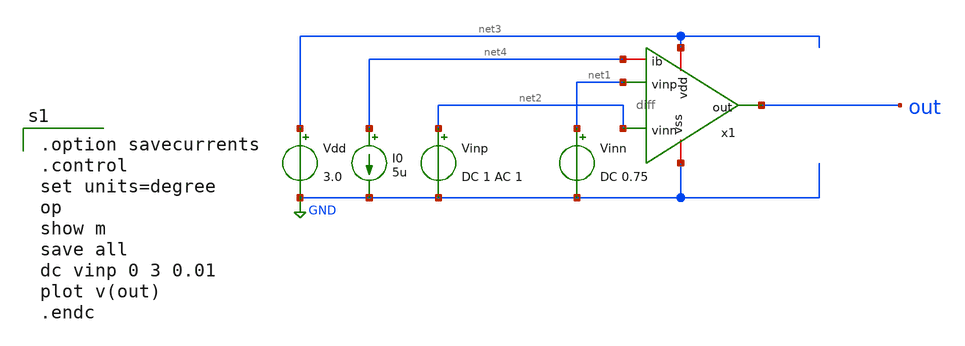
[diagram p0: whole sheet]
** sch_path: member_project/DCDC/ShuntaroOHNO/xschem/diff_dc.sch
**.subckt diff_dc
Vinn net1 GND DC 0.75
Vinp net2 GND DC 1 AC 1
Vdd net3 GND 3.0
I0 net4 GND 5u
x1 net3 net4 net2 out net1 GND diff
**** begin user architecture code
 .include $::LIB/ip62_models

.option savecurrents
.control
set units=degree
op
show m
save all
dc vinp 0 3 0.01
plot v(out)
.endc

**** end user architecture code
**.ends
.GLOBAL GND
.end
